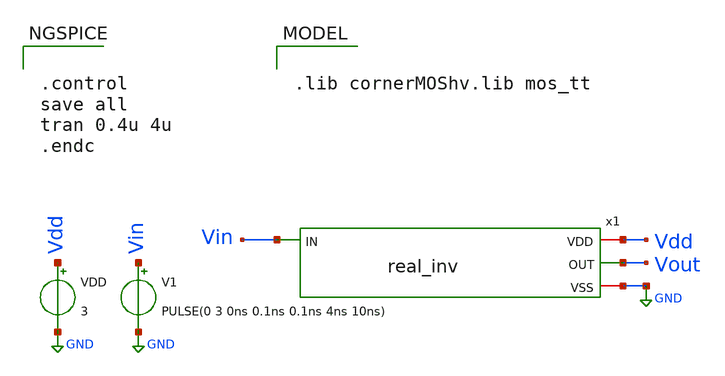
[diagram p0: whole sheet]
** sch_path: real_circuit/inv_tb.sch
**.subckt inv_tb
VDD Vdd GND 3
x1 Vdd Vin Vout GND real_inv
V1 Vin GND PULSE(0 3 0ns 0.1ns 0.1ns 4ns 10ns)
**** begin user architecture code


.control
save all
tran 0.4u 4u
.endc



.lib cornerMOShv.lib mos_tt

**** end user architecture code
**.ends

* expanding   symbol:  /foss/designs/delta_sigma/real/real_inv.sym # of pins=4
** sym_path: real_circuit/real_inv.sym
** sch_path: real_circuit/real_inv.sch
.subckt real_inv VDD IN OUT VSS
*.iopin VDD
*.iopin VSS
*.ipin IN
*.opin OUT
XM1 OUT IN VDD VDD sg13_hv_pmos w=0.6u l=0.4u ng=1 m=1 mm_ok=1
XM2 OUT IN VSS VSS sg13_hv_nmos w=0.3u l=0.45u ng=1 m=1 mm_ok=1
.ends

.GLOBAL GND
.end
